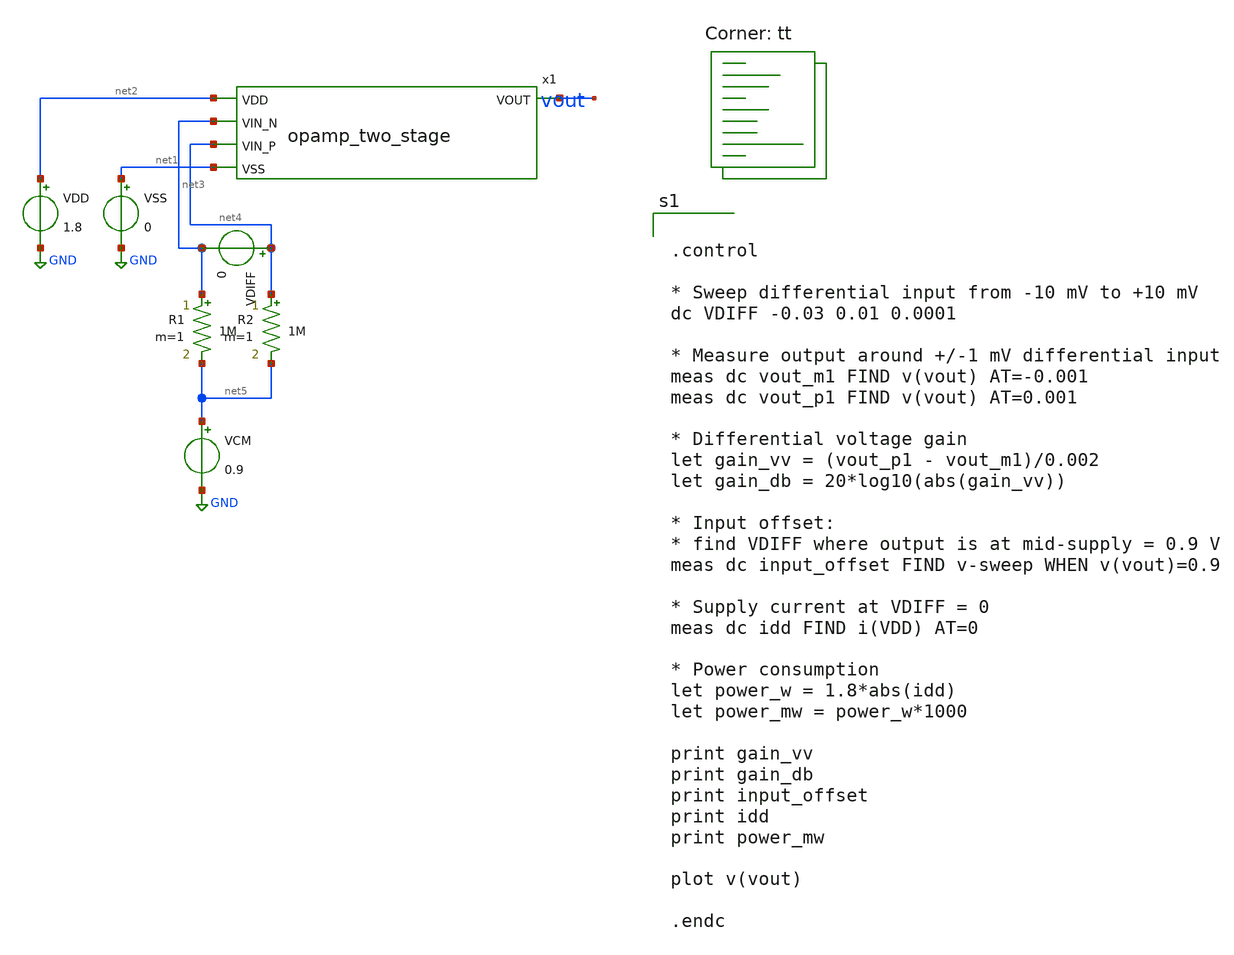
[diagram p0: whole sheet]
** sch_path: analog/build/schematic/tb_dc_analysis.sch
**.subckt tb_dc_analysis
VSS net1 GND 0
VDD net2 GND 1.8
VDIFF net4 net3 0
R1 net3 net5 1M m=1
R2 net4 net5 1M m=1
VCM net5 GND 0.9
x1 net2 vout net3 net4 net1 opamp_two_stage
**** begin user architecture code
.lib $::SKYWATER_MODELS/sky130.lib.spice tt


.control

* Sweep differential input from -10 mV to +10 mV
dc VDIFF -0.03 0.01 0.0001

* Measure output around +/-1 mV differential input
meas dc vout_m1 FIND v(vout) AT=-0.001
meas dc vout_p1 FIND v(vout) AT=0.001

* Differential voltage gain
let gain_vv = (vout_p1 - vout_m1)/0.002
let gain_db = 20*log10(abs(gain_vv))

* Input offset:
* find VDIFF where output is at mid-supply = 0.9 V
meas dc input_offset FIND v-sweep WHEN v(vout)=0.9

* Supply current at VDIFF = 0
meas dc idd FIND i(VDD) AT=0

* Power consumption
let power_w = 1.8*abs(idd)
let power_mw = power_w*1000

print gain_vv
print gain_db
print input_offset
print idd
print power_mw

plot v(vout)

.endc


**** end user architecture code
**.ends

* expanding   symbol:  opamp_two_stage.sym # of pins=5
** sym_path: analog/build/schematic/opamp_two_stage.sym
** sch_path: analog/build/schematic/opamp_two_stage.sch
.subckt opamp_two_stage VDD VOUT VIN_N VIN_P VSS
*.ipin VIN_N
*.ipin VIN_P
*.opin VOUT
*.ipin VDD
*.ipin VSS
XM1 net3 VIN_N net1 VSS sky130_fd_pr__nfet_01v8 L=1 W=10 nf=1 ad='int((nf+1)/2) * W/nf * 0.29' as='int((nf+2)/2) * W/nf * 0.29'
+ pd='2*int((nf+1)/2) * (W/nf + 0.29)' ps='2*int((nf+2)/2) * (W/nf + 0.29)' nrd='0.29 / W' nrs='0.29 / W'
+ sa=0 sb=0 sd=0 mult=1 m=1
XM2 net2 VIN_P net1 VSS sky130_fd_pr__nfet_01v8 L=1 W=10 nf=1 ad='int((nf+1)/2) * W/nf * 0.29' as='int((nf+2)/2) * W/nf * 0.29'
+ pd='2*int((nf+1)/2) * (W/nf + 0.29)' ps='2*int((nf+2)/2) * (W/nf + 0.29)' nrd='0.29 / W' nrs='0.29 / W'
+ sa=0 sb=0 sd=0 mult=1 m=1
XM3 net1 net5 VSS VSS sky130_fd_pr__nfet_01v8 L=2 W=10 nf=1 ad='int((nf+1)/2) * W/nf * 0.29' as='int((nf+2)/2) * W/nf * 0.29'
+ pd='2*int((nf+1)/2) * (W/nf + 0.29)' ps='2*int((nf+2)/2) * (W/nf + 0.29)' nrd='0.29 / W' nrs='0.29 / W'
+ sa=0 sb=0 sd=0 mult=1 m=1
XM4 net3 net2 VDD VDD sky130_fd_pr__pfet_01v8 L=1 W=20 nf=1 ad='int((nf+1)/2) * W/nf * 0.29' as='int((nf+2)/2) * W/nf * 0.29'
+ pd='2*int((nf+1)/2) * (W/nf + 0.29)' ps='2*int((nf+2)/2) * (W/nf + 0.29)' nrd='0.29 / W' nrs='0.29 / W'
+ sa=0 sb=0 sd=0 mult=1 m=1
XM5 net2 net2 VDD VDD sky130_fd_pr__pfet_01v8 L=1 W=20 nf=1 ad='int((nf+1)/2) * W/nf * 0.29' as='int((nf+2)/2) * W/nf * 0.29'
+ pd='2*int((nf+1)/2) * (W/nf + 0.29)' ps='2*int((nf+2)/2) * (W/nf + 0.29)' nrd='0.29 / W' nrs='0.29 / W'
+ sa=0 sb=0 sd=0 mult=1 m=1
XM7 VOUT net5 VSS VSS sky130_fd_pr__nfet_01v8 L=2 W=10 nf=1 ad='int((nf+1)/2) * W/nf * 0.29' as='int((nf+2)/2) * W/nf * 0.29'
+ pd='2*int((nf+1)/2) * (W/nf + 0.29)' ps='2*int((nf+2)/2) * (W/nf + 0.29)' nrd='0.29 / W' nrs='0.29 / W'
+ sa=0 sb=0 sd=0 mult=1 m=1
XM8 VOUT net3 VDD VDD sky130_fd_pr__pfet_01v8 L=1 W=20 nf=1 ad='int((nf+1)/2) * W/nf * 0.29' as='int((nf+2)/2) * W/nf * 0.29'
+ pd='2*int((nf+1)/2) * (W/nf + 0.29)' ps='2*int((nf+2)/2) * (W/nf + 0.29)' nrd='0.29 / W' nrs='0.29 / W'
+ sa=0 sb=0 sd=0 mult=1 m=1
C1 net3 net4 1p m=1
R1 VOUT net4 2k m=1
XM_bias net5 net5 VSS VSS sky130_fd_pr__nfet_01v8 L=2 W=10 nf=1 ad='int((nf+1)/2) * W/nf * 0.29' as='int((nf+2)/2) * W/nf * 0.29'
+ pd='2*int((nf+1)/2) * (W/nf + 0.29)' ps='2*int((nf+2)/2) * (W/nf + 0.29)' nrd='0.29 / W' nrs='0.29 / W'
+ sa=0 sb=0 sd=0 mult=1 m=1
R2 VDD net5 10k m=1
.ends

.GLOBAL GND
.end
